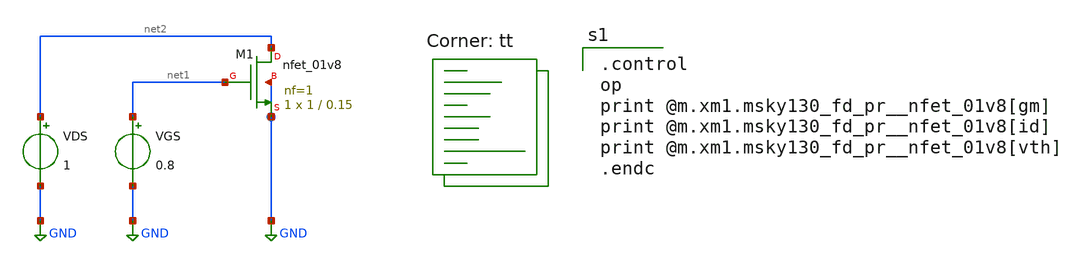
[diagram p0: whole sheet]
** sch_path: analog/gm-ID-LUT/schematics/test_nfet.sch
**.subckt test_nfet
XM1 net2 net1 GND GND sky130_fd_pr__nfet_01v8 L=0.15 W=1 nf=1 ad='int((nf+1)/2) * W/nf * 0.29' as='int((nf+2)/2) * W/nf * 0.29'
+ pd='2*int((nf+1)/2) * (W/nf + 0.29)' ps='2*int((nf+2)/2) * (W/nf + 0.29)' nrd='0.29 / W' nrs='0.29 / W'
+ sa=0 sb=0 sd=0 mult=1 m=1
VDS net2 GND 1
VGS net1 GND 0.8
**** begin user architecture code
.lib $::SKYWATER_MODELS/sky130.lib.spice tt

.control
op
print @m.xm1.msky130_fd_pr__nfet_01v8[gm]
print @m.xm1.msky130_fd_pr__nfet_01v8[id]
print @m.xm1.msky130_fd_pr__nfet_01v8[vth]
.endc


**** end user architecture code
**.ends
.GLOBAL GND
.end
